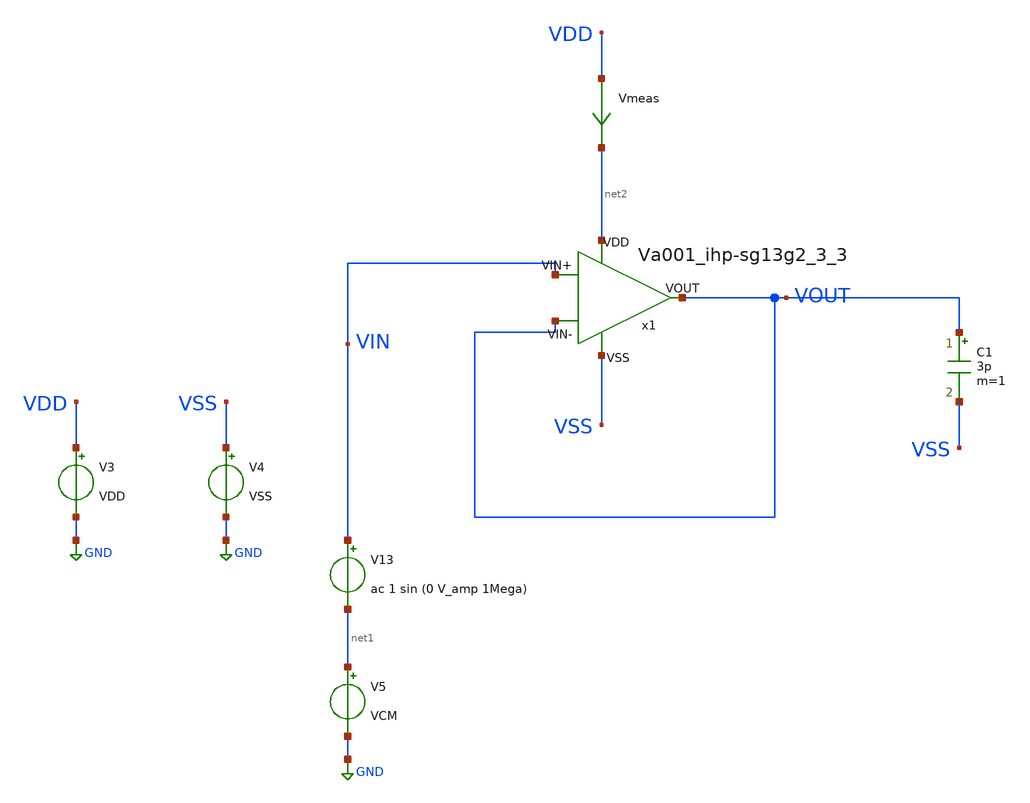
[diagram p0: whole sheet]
** sch_path: Learning/single_ended_amplifiers/VA001_series/Design_and_Analysis_of_Two-Stage_CMOS_Operational_Amplifier_for_Fluorescence_Signal_Processing_ihp130_3_3V/amplifier_design/swing.sch
**.subckt swing
Vmeas VDD net2 0
.save i(vmeas)
C1 VOUT VSS 3p m=1
V5 net1 GND VCM
V13 VIN net1 ac 1 sin (0 V_amp 1Mega)
V3 VDD GND VDD
V4 VSS GND VSS
x1 net2 VSS VOUT VIN VOUT Va001_ihp-sg13g2_3_3
**** begin user architecture code

.lib $::SG13G2_MODELS/cornerRES.lib res_typ


.lib cornerMOShv.lib mos_tt


.lib $::SG13G2_MODELS/cornerCAP.lib cap_typ

**** end user architecture code
**.ends

* expanding   symbol:  ihp-sg13g2/Amplifiers/Va001_ihp-sg13g2_3_3.sym # of pins=5
** sym_path: LIB/ihp-sg13g2/Amplifiers/Va001_ihp-sg13g2_3_3.sym
** sch_path: LIB/ihp-sg13g2/Amplifiers/Va001_ihp-sg13g2_3_3.sch
.subckt Va001_ihp-sg13g2_3_3 VDD VSS VIN- VIN+ VOUT
*.iopin VDD
*.iopin VSS
*.iopin VIN-
*.iopin VIN+
*.iopin VOUT
XM2 VB1 VB1 VDD VDD sg13_hv_pmos w=1.5u l=2u ng=2 m=2 mm_ok=1
XM1 VB2 VB1 VDD VDD sg13_hv_pmos w=1.5u l=2u ng=2 m=2 mm_ok=1
XM3 VB1 VB2 net3 VSS sg13_hv_nmos w=1.0u l=2u ng=2 m=2 mm_ok=1
XM4 VB2 VB2 net1 VSS sg13_hv_nmos w=1.0u l=2u ng=2 m=2 mm_ok=1
XM5 net3 net1 net2 VSS sg13_hv_nmos w=2u l=2u ng=2 m=8 mm_ok=1
XM6 net1 net1 VSS VSS sg13_hv_nmos w=2u l=2u ng=2 m=2 mm_ok=1
XR1 net2 VSS sub! rhigh w=0.5e-6 l=5.9e-6 m=1 b=0 mm_ok=1
XM7 net4 VB1 VDD VDD sg13_hv_pmos w=1.5u l=2u ng=2 m=8 mm_ok=1
XM9 net6 VIN+ net4 net4 sg13_hv_pmos w=8u l=0.8u ng=4 m=4 mm_ok=1
XM8 net5 VIN- net4 net4 sg13_hv_pmos w=8u l=0.8u ng=4 m=4 mm_ok=1
XM10 net5 net5 VSS VSS sg13_hv_nmos w=2u l=2u ng=2 m=2 mm_ok=1
XM11 net6 net5 VSS VSS sg13_hv_nmos w=2u l=2u ng=2 m=2 mm_ok=1
XM12 VOUT VB1 VDD VDD sg13_hv_pmos w=1.5u l=2u ng=2 m=16 mm_ok=1
XM13 VOUT net6 VSS VSS sg13_hv_nmos w=2u l=0.8u ng=2 m=4 mm_ok=1
XM14 net6 VB2 net7 VSS sg13_hv_nmos w=2u l=2.7u ng=1 m=2 mm_ok=1
XC1 VOUT net7 cap_cmim w=9e-6 l=9e-6 m=4 mm_ok=1
.ends

.GLOBAL GND
**** begin user architecture code


.Temp 27
.param VDD = 3.3
.param VCM = 1.65
.param V_amp = 1.1
.param VSS = 0
.param CL = 3p


.control

	save all
	tran 100p 5u
	plot v(VOUT) v(VIN)

.endc



**** end user architecture code
.end
